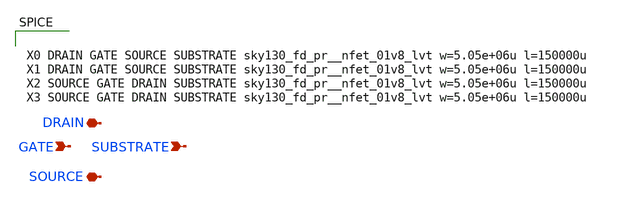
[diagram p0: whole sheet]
** sch_path: xschem/rf_nfet_01v8_lvt_aM04W5p00L0p15.sch
**.subckt rf_nfet_01v8_lvt_aM04W5p00L0p15 SOURCE DRAIN GATE SUBSTRATE
*.iopin SOURCE
*.iopin DRAIN
*.ipin GATE
*.ipin SUBSTRATE
**** begin user architecture code


X0 DRAIN GATE SOURCE SUBSTRATE sky130_fd_pr__nfet_01v8_lvt w=5.05e+06u l=150000u
X1 DRAIN GATE SOURCE SUBSTRATE sky130_fd_pr__nfet_01v8_lvt w=5.05e+06u l=150000u
X2 SOURCE GATE DRAIN SUBSTRATE sky130_fd_pr__nfet_01v8_lvt w=5.05e+06u l=150000u
X3 SOURCE GATE DRAIN SUBSTRATE sky130_fd_pr__nfet_01v8_lvt w=5.05e+06u l=150000u


**** end user architecture code
**.ends
.end
